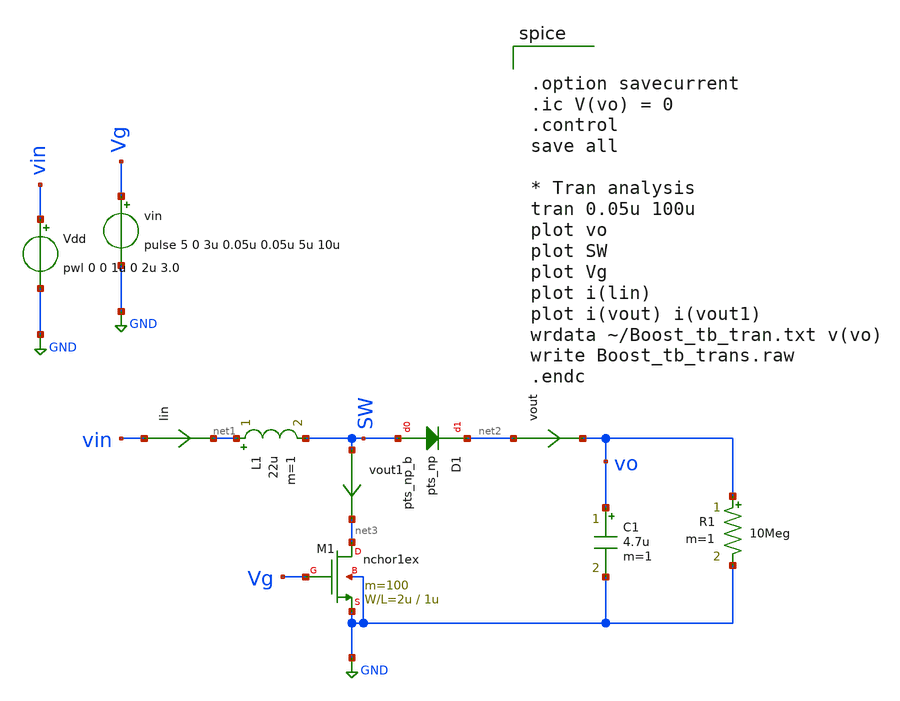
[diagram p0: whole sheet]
** sch_path: design/xschem/BoostDCDC_diode.sch
**.subckt BoostDCDC_diode
M1 net3 Vg GND GND nchor1ex L=1u W=2u m=100
L1 net1 SW 22u m=1
C1 vo GND 4.7u m=1
Vdd vin GND pwl 0 0 1u 0 2u 3.0
vin Vg GND pulse 5 0 3u 0.05u 0.05u 5u 10u
lin vin net1 0
.save i(lin)
R1 vo GND 10Meg m=1
vout net2 vo 0
.save i(vout)
D1 SW net2 pts_np_b area=100e-12
vout1 SW net3 0
.save i(vout1)
**** begin user architecture code


.option savecurrent
.ic V(vo) = 0
.control
save all

* Tran analysis
tran 0.05u 100u
plot vo
plot SW
plot Vg
plot i(lin)
plot i(vout) i(vout1)
wrdata ~/Boost_tb_tran.txt v(vo)
write Boost_tb_trans.raw
.endc

 .include $::LIB/mos.lib
.include $::LIB/passive.lib
.include $::LIB/diode.lib
**** end user architecture code
**.ends
.GLOBAL GND
.end
